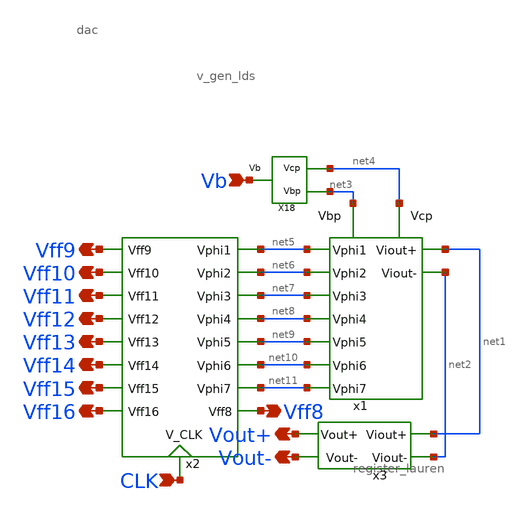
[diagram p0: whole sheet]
** sch_path: simulation/post_layout_sim/final.sch
**.subckt final Vb Vff9 Vff10 Vff11 Vff12 Vff13 Vff14 Vff15 Vff16 CLK Vff8 Vout+ Vout-
*.ipin Vb
*.opin Vff9
*.opin Vff10
*.opin Vff11
*.opin Vff12
*.opin Vff13
*.opin Vff14
*.opin Vff15
*.opin Vff16
*.ipin CLK
*.opin Vff8
*.opin Vout+
*.opin Vout-
x2 Vff10 Vff11 Vff12 Vff13 Vff14 Vff16 Vff15 Vff9 net5 net6 net7 net8 net9 net10 net11 Vff8 CLK
+ register_lauren
X18 net4 net3 Vb v_gen_lds
x3 net1 net2 Vout+ Vout- filter_lvs
x1 net5 net6 net7 net8 net9 net10 net11 net1 net2 net3 net4 dac
**.ends
.end
